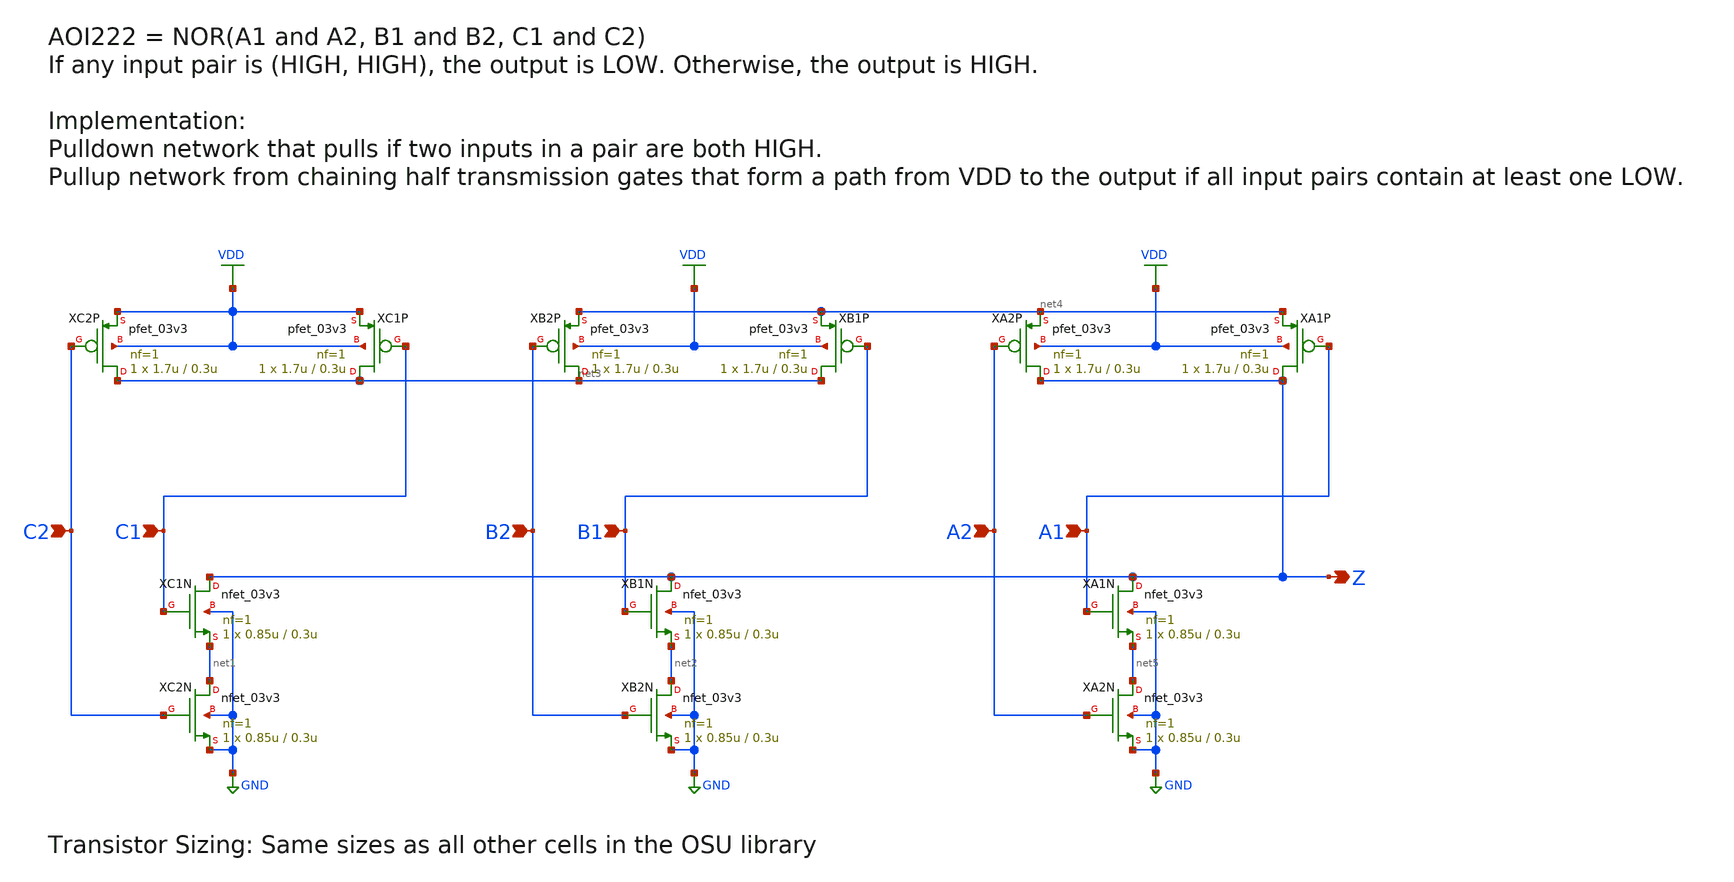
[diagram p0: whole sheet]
** sch_path: globalfoundries-pdk-libs-gf180mcu_sah_sc/cells/aoi222/gf180mcu_sah_sc_aoi222_1.sch
**.subckt gf180mcu_sah_sc_aoi222_1 C1 C2 B1 B2 Z A1 A2
*.ipin C1
*.ipin C2
*.ipin B1
*.ipin B2
*.opin Z
*.ipin A1
*.ipin A2
XC1N Z C1 net1 GND nfet_03v3 L=0.3u W=0.85u nf=1 ad='int((nf+1)/2) * W/nf * 0.18u' as='int((nf+2)/2) * W/nf * 0.18u'
+ pd='2*int((nf+1)/2) * (W/nf + 0.18u)' ps='2*int((nf+2)/2) * (W/nf + 0.18u)' nrd='0.18u / W' nrs='0.18u / W'
+ sa=0 sb=0 sd=0 m=1
XC2N net1 C2 GND GND nfet_03v3 L=0.3u W=0.85u nf=1 ad='int((nf+1)/2) * W/nf * 0.18u' as='int((nf+2)/2) * W/nf * 0.18u'
+ pd='2*int((nf+1)/2) * (W/nf + 0.18u)' ps='2*int((nf+2)/2) * (W/nf + 0.18u)' nrd='0.18u / W' nrs='0.18u / W'
+ sa=0 sb=0 sd=0 m=1
XC1P net3 C1 VDD VDD pfet_03v3 L=0.3u W=1.7u nf=1 ad='int((nf+1)/2) * W/nf * 0.18u' as='int((nf+2)/2) * W/nf * 0.18u'
+ pd='2*int((nf+1)/2) * (W/nf + 0.18u)' ps='2*int((nf+2)/2) * (W/nf + 0.18u)' nrd='0.18u / W' nrs='0.18u / W'
+ sa=0 sb=0 sd=0 m=1
XC2P net3 C2 VDD VDD pfet_03v3 L=0.3u W=1.7u nf=1 ad='int((nf+1)/2) * W/nf * 0.18u' as='int((nf+2)/2) * W/nf * 0.18u'
+ pd='2*int((nf+1)/2) * (W/nf + 0.18u)' ps='2*int((nf+2)/2) * (W/nf + 0.18u)' nrd='0.18u / W' nrs='0.18u / W'
+ sa=0 sb=0 sd=0 m=1
XB1N Z B1 net2 GND nfet_03v3 L=0.3u W=0.85u nf=1 ad='int((nf+1)/2) * W/nf * 0.18u' as='int((nf+2)/2) * W/nf * 0.18u'
+ pd='2*int((nf+1)/2) * (W/nf + 0.18u)' ps='2*int((nf+2)/2) * (W/nf + 0.18u)' nrd='0.18u / W' nrs='0.18u / W'
+ sa=0 sb=0 sd=0 m=1
XB2N net2 B2 GND GND nfet_03v3 L=0.3u W=0.85u nf=1 ad='int((nf+1)/2) * W/nf * 0.18u' as='int((nf+2)/2) * W/nf * 0.18u'
+ pd='2*int((nf+1)/2) * (W/nf + 0.18u)' ps='2*int((nf+2)/2) * (W/nf + 0.18u)' nrd='0.18u / W' nrs='0.18u / W'
+ sa=0 sb=0 sd=0 m=1
XB1P net3 B1 net4 VDD pfet_03v3 L=0.3u W=1.7u nf=1 ad='int((nf+1)/2) * W/nf * 0.18u' as='int((nf+2)/2) * W/nf * 0.18u'
+ pd='2*int((nf+1)/2) * (W/nf + 0.18u)' ps='2*int((nf+2)/2) * (W/nf + 0.18u)' nrd='0.18u / W' nrs='0.18u / W'
+ sa=0 sb=0 sd=0 m=1
XB2P net3 B2 net4 VDD pfet_03v3 L=0.3u W=1.7u nf=1 ad='int((nf+1)/2) * W/nf * 0.18u' as='int((nf+2)/2) * W/nf * 0.18u'
+ pd='2*int((nf+1)/2) * (W/nf + 0.18u)' ps='2*int((nf+2)/2) * (W/nf + 0.18u)' nrd='0.18u / W' nrs='0.18u / W'
+ sa=0 sb=0 sd=0 m=1
XA1N Z A1 net5 GND nfet_03v3 L=0.3u W=0.85u nf=1 ad='int((nf+1)/2) * W/nf * 0.18u' as='int((nf+2)/2) * W/nf * 0.18u'
+ pd='2*int((nf+1)/2) * (W/nf + 0.18u)' ps='2*int((nf+2)/2) * (W/nf + 0.18u)' nrd='0.18u / W' nrs='0.18u / W'
+ sa=0 sb=0 sd=0 m=1
XA2N net5 A2 GND GND nfet_03v3 L=0.3u W=0.85u nf=1 ad='int((nf+1)/2) * W/nf * 0.18u' as='int((nf+2)/2) * W/nf * 0.18u'
+ pd='2*int((nf+1)/2) * (W/nf + 0.18u)' ps='2*int((nf+2)/2) * (W/nf + 0.18u)' nrd='0.18u / W' nrs='0.18u / W'
+ sa=0 sb=0 sd=0 m=1
XA1P Z A1 net4 VDD pfet_03v3 L=0.3u W=1.7u nf=1 ad='int((nf+1)/2) * W/nf * 0.18u' as='int((nf+2)/2) * W/nf * 0.18u'
+ pd='2*int((nf+1)/2) * (W/nf + 0.18u)' ps='2*int((nf+2)/2) * (W/nf + 0.18u)' nrd='0.18u / W' nrs='0.18u / W'
+ sa=0 sb=0 sd=0 m=1
XA2P Z A2 net4 VDD pfet_03v3 L=0.3u W=1.7u nf=1 ad='int((nf+1)/2) * W/nf * 0.18u' as='int((nf+2)/2) * W/nf * 0.18u'
+ pd='2*int((nf+1)/2) * (W/nf + 0.18u)' ps='2*int((nf+2)/2) * (W/nf + 0.18u)' nrd='0.18u / W' nrs='0.18u / W'
+ sa=0 sb=0 sd=0 m=1
**.ends
.GLOBAL GND
.GLOBAL VDD
.end
